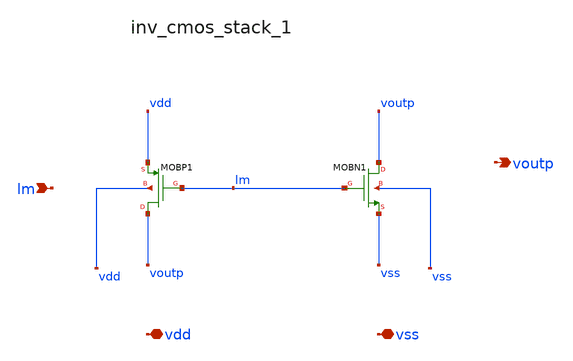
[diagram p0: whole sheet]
** sch_path: analog-db/raw/cmp_002_strongarm/hier/blocks/inv_cmos_stack_1.sch
**.subckt inv_cmos_stack_1 lm vdd vss voutp
*.ipin lm
*.iopin vdd
*.iopin vss
*.opin voutp
XMOBN1 voutp lm vss vss sg13_lv_nmos w=x_dut_xmobn1_w l=x_dut_xmobn1_l ng=1 m=x_dut_xmobn1_m
XMOBP1 voutp lm vdd vdd sg13_lv_pmos w=x_dut_xmobp1_w l=x_dut_xmobp1_l ng=1 m=x_dut_xmobp1_m
**.ends
.end
